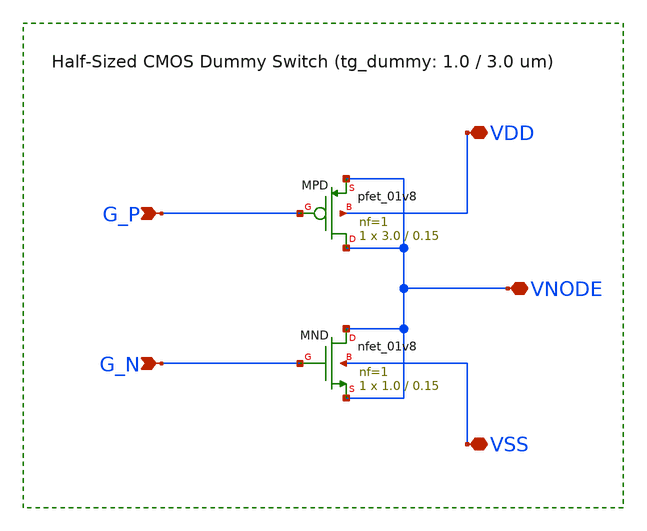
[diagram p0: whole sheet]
** sch_path: sky130-sc-lpf/xschem/tg_dummy.sch
**.subckt tg_dummy VNODE G_P G_N VDD VSS
*.iopin VNODE
*.ipin G_P
*.ipin G_N
*.iopin VDD
*.iopin VSS
XMPD VNODE G_P VNODE VDD sky130_fd_pr__pfet_01v8 L=0.15 W=3.0 nf=1 ad='int((nf+1)/2) * W/nf * 0.29' as='int((nf+2)/2) * W/nf * 0.29'
+ pd='2*int((nf+1)/2) * (W/nf + 0.29)' ps='2*int((nf+2)/2) * (W/nf + 0.29)' nrd='0.29 / W' nrs='0.29 / W'
+ sa=0 sb=0 sd=0 mult=1 m=1
XMND VNODE G_N VNODE VSS sky130_fd_pr__nfet_01v8 L=0.15 W=1.0 nf=1 ad='int((1 + 1)/2) * 1.0 / 1 * 0.29'
+ as='int((1 + 2)/2) * 1.0 / 1 * 0.29' pd='2*int((1 + 1)/2) * (1.0 / 1 + 0.29)' ps='2*int((1 + 2)/2) * (1.0 / 1 + 0.29)'
+ nrd='0.29 / 1.0 ' nrs='0.29 / 1.0 ' sa=0 sb=0 sd=0 mult=1 m=1
**.ends
.end
